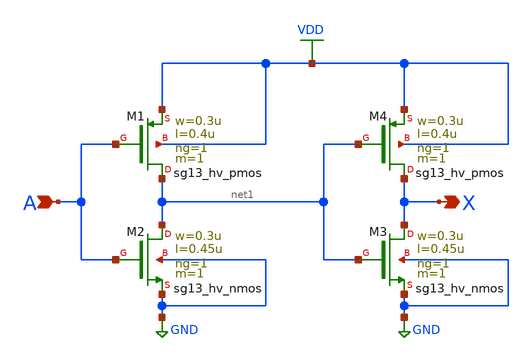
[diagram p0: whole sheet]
** sch_path: 3_real_circuits/buffer.sch
**.subckt buffer A X
*.ipin A
*.opin X
XM2 net1 A GND GND sg13_hv_nmos w=0.3u l=0.45u ng=1 m=1 mm_ok=1
XM1 net1 A VDD VDD sg13_hv_pmos w=0.3u l=0.4u ng=1 m=1 mm_ok=1
XM3 X net1 GND GND sg13_hv_nmos w=0.3u l=0.45u ng=1 m=1 mm_ok=1
XM4 X net1 VDD VDD sg13_hv_pmos w=0.3u l=0.4u ng=1 m=1 mm_ok=1
**.ends
.GLOBAL GND
.GLOBAL VDD
.end
